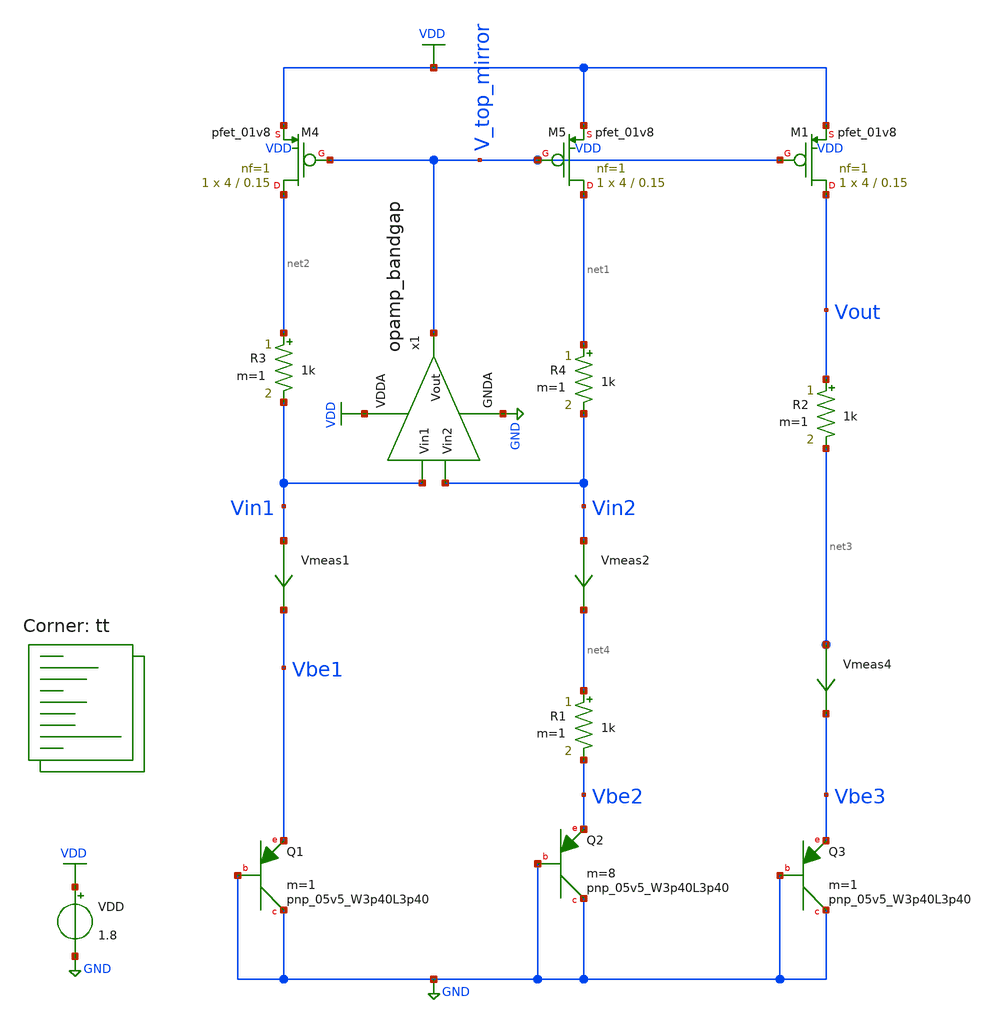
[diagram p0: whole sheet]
** sch_path: projects/pll/bandgapref/xschem_ngspice/mos_bandgap3.sch
**.subckt mos_bandgap3
XM4 net2 V_top_mirror VDD VDD sky130_fd_pr__pfet_01v8 L=0.15 W=4 nf=1 ad='int((nf+1)/2) * W/nf * 0.29'
+ as='int((nf+2)/2) * W/nf * 0.29' pd='2*int((nf+1)/2) * (W/nf + 0.29)' ps='2*int((nf+2)/2) * (W/nf + 0.29)'
+ nrd='0.29 / W' nrs='0.29 / W' sa=0 sb=0 sd=0 mult=1 m=1
XM5 net1 V_top_mirror VDD VDD sky130_fd_pr__pfet_01v8 L=0.15 W=4 nf=1 ad='int((nf+1)/2) * W/nf * 0.29'
+ as='int((nf+2)/2) * W/nf * 0.29' pd='2*int((nf+1)/2) * (W/nf + 0.29)' ps='2*int((nf+2)/2) * (W/nf + 0.29)'
+ nrd='0.29 / W' nrs='0.29 / W' sa=0 sb=0 sd=0 mult=1 m=1
VDD VDD GND 1.8
R1 net4 Vbe2 1k m=1
XQ1 GND GND Vbe1 sky130_fd_pr__pnp_05v5_W3p40L3p40 m=1
XQ2 GND GND Vbe2 sky130_fd_pr__pnp_05v5_W3p40L3p40 m=8
XM1 Vout V_top_mirror VDD VDD sky130_fd_pr__pfet_01v8 L=0.15 W=4 nf=1 ad='int((nf+1)/2) * W/nf * 0.29'
+ as='int((nf+2)/2) * W/nf * 0.29' pd='2*int((nf+1)/2) * (W/nf + 0.29)' ps='2*int((nf+2)/2) * (W/nf + 0.29)'
+ nrd='0.29 / W' nrs='0.29 / W' sa=0 sb=0 sd=0 mult=1 m=1
R2 Vout net3 1k m=1
XQ3 GND GND Vbe3 sky130_fd_pr__pnp_05v5_W3p40L3p40 m=1
Vmeas4 net3 Vbe3 0
.save i(vmeas4)
x1 VDD V_top_mirror Vin2 Vin1 GND opamp_bandgap
R3 net2 Vin1 1k m=1
R4 net1 Vin2 1k m=1
Vmeas1 Vin1 Vbe1 0
.save i(vmeas1)
Vmeas2 Vin2 net4 0
.save i(vmeas2)
**** begin user architecture code
.lib $::SKYWATER_MODELS/sky130.lib.spice tt



.option wnflag=1

* .param VDDGAUSS = agauss(1.8, 0.05, 1)
* .param VDD = VDDGAUSS
.param VDD = 1.8

* .param TEMPGAUSS = agauss(40, 30, 1)
* .param temp = TEMPGAUSS
.option temp = 26

.control
  save all
  op
  dc temp -40 120 1 VDD 3 6 0.1
  write mos_bandgap3.raw
  set appendwrite
.endc



**** end user architecture code
**.ends

* expanding   symbol:
*+  /foss/designs/my_design/projects/pll/bandgapref/xschem_ngspice/opamp_bandgap.sym # of pins=5
** sym_path: projects/pll/bandgapref/xschem_ngspice/opamp_bandgap.sym
** sch_path: projects/pll/bandgapref/xschem_ngspice/opamp_bandgap.sch
.subckt opamp_bandgap VDDA Vout Vin2 Vin1 GNDA
*.ipin Vin1
*.opin Vout
*.ipin Vin2
*.ipin GNDA
*.ipin VDDA
XM2 net1 Vin1 net2 GNDA sky130_fd_pr__nfet_01v8 L=0.15 W=1 nf=1 ad='int((nf+1)/2) * W/nf * 0.29' as='int((nf+2)/2) * W/nf * 0.29'
+ pd='2*int((nf+1)/2) * (W/nf + 0.29)' ps='2*int((nf+2)/2) * (W/nf + 0.29)' nrd='0.29 / W' nrs='0.29 / W'
+ sa=0 sb=0 sd=0 mult=1 m=1
XM3 Vout Vin2 net2 GNDA sky130_fd_pr__nfet_01v8 L=0.15 W=1 nf=1 ad='int((nf+1)/2) * W/nf * 0.29' as='int((nf+2)/2) * W/nf * 0.29'
+ pd='2*int((nf+1)/2) * (W/nf + 0.29)' ps='2*int((nf+2)/2) * (W/nf + 0.29)' nrd='0.29 / W' nrs='0.29 / W'
+ sa=0 sb=0 sd=0 mult=1 m=1
XM4 net1 net1 VDDA VDDA sky130_fd_pr__pfet_01v8 L=0.15 W=2 nf=1 ad='int((nf+1)/2) * W/nf * 0.29' as='int((nf+2)/2) * W/nf * 0.29'
+ pd='2*int((nf+1)/2) * (W/nf + 0.29)' ps='2*int((nf+2)/2) * (W/nf + 0.29)' nrd='0.29 / W' nrs='0.29 / W'
+ sa=0 sb=0 sd=0 mult=1 m=1
XM5 Vout net1 VDDA VDDA sky130_fd_pr__pfet_01v8 L=0.15 W=2 nf=1 ad='int((nf+1)/2) * W/nf * 0.29' as='int((nf+2)/2) * W/nf * 0.29'
+ pd='2*int((nf+1)/2) * (W/nf + 0.29)' ps='2*int((nf+2)/2) * (W/nf + 0.29)' nrd='0.29 / W' nrs='0.29 / W'
+ sa=0 sb=0 sd=0 mult=1 m=1
XM1 net2 net2 GNDA GNDA sky130_fd_pr__nfet_01v8 L=0.15 W=1 nf=1 ad='int((nf+1)/2) * W/nf * 0.29' as='int((nf+2)/2) * W/nf * 0.29'
+ pd='2*int((nf+1)/2) * (W/nf + 0.29)' ps='2*int((nf+2)/2) * (W/nf + 0.29)' nrd='0.29 / W' nrs='0.29 / W'
+ sa=0 sb=0 sd=0 mult=1 m=1
.ends

.GLOBAL GND
.GLOBAL VDD
.end
